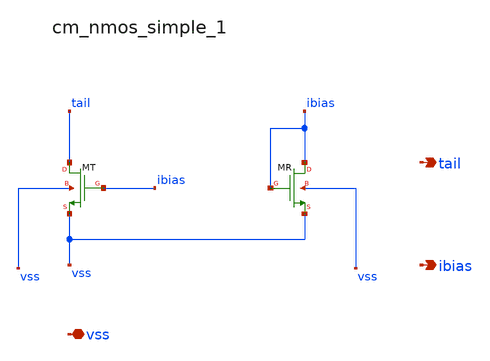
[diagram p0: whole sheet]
** sch_path: analog-db/raw/dp_001_resistive_load/hier/blocks/cm_nmos_simple_1.sch
**.subckt cm_nmos_simple_1 vss tail ibias
*.iopin vss
*.opin tail
*.opin ibias
XMR ibias ibias vss vss sg13_lv_nmos w=x_dut_xmr_w l=x_dut_xmr_l ng=1 m=x_dut_xmr_m
XMT tail ibias vss vss sg13_lv_nmos w=x_dut_xmt_w l=x_dut_xmt_l ng=1 m=x_dut_xmt_m
**.ends
.end
